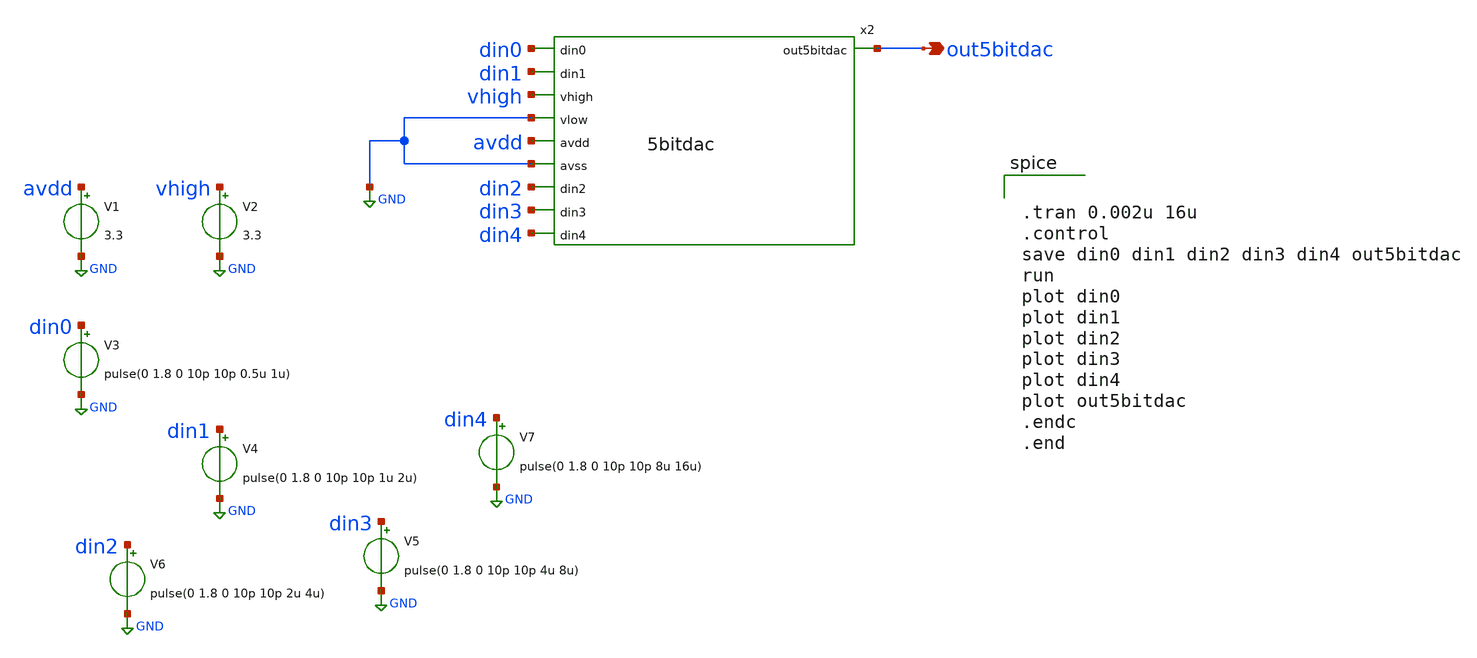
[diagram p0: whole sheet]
** sch_path: xschem/tb_5bitdac_fast.sch
**.subckt tb_5bitdac_fast out5bitdac
*.opin out5bitdac
V1 avdd GND 3.3
V2 vhigh GND 3.3
V3 din0 GND pulse(0 1.8 0 10p 10p 0.5u 1u)
V4 din1 GND pulse(0 1.8 0 10p 10p 1u 2u)
V5 din3 GND pulse(0 1.8 0 10p 10p 4u 8u)
V6 din2 GND pulse(0 1.8 0 10p 10p 2u 4u)
V7 din4 GND pulse(0 1.8 0 10p 10p 8u 16u)
x2 out5bitdac din0 din1 vhigh GND avdd GND din2 din3 din4 5bitdac
**** begin user architecture code

** opencircuitdesign pdks install
.lib $::SKYWATER_MODELS/sky130.lib.spice tt




.tran 0.002u 16u
.control
save din0 din1 din2 din3 din4 out5bitdac
run
plot din0
plot din1
plot din2
plot din3
plot din4
plot out5bitdac
.endc
.end

**** end user architecture code
**.ends

* expanding   symbol:  5bitdac.sym # of pins=10
** sym_path: xschem/5bitdac.sym
** sch_path: xschem/5bitdac.sch
.subckt 5bitdac out5bitdac din0 din1 vhigh vlow avdd avss din2 din3 din4
*.ipin din0
*.ipin din1
*.ipin vhigh
*.ipin vlow
*.ipin avdd
*.ipin avss
*.ipin din2
*.ipin din3
*.opin out5bitdac
*.ipin din4
x1 x1out din0 din1 vhigh net2 avdd avss din2 din3 4bitdac
x2 x2out din0 din1 net1 vlow avdd avss din2 din3 4bitdac
x3 out5bitdac x1out x2out avss avdd din4 switch
XR6 net1 net2 avss sky130_fd_pr__res_high_po_0p35 L=3 mult=1 m=1
.ends


* expanding   symbol:  4bitdac.sym # of pins=9
** sym_path: xschem/4bitdac.sym
** sch_path: xschem/4bitdac.sch
.subckt 4bitdac out4bitdac din0 din1 vhigh vlow avdd avss din2 din3
*.ipin din0
*.ipin din1
*.ipin vhigh
*.ipin vlow
*.ipin avdd
*.ipin avss
*.ipin din2
*.ipin din3
*.opin out4bitdac
x1 x1out din0 din1 vhigh net1 avdd avss din2 3bitdac
x2 x2out din0 din1 net2 vlow avdd avss din2 3bitdac
x3 out4bitdac x1out x2out avss avdd din3 switch
XR6 net2 net1 avss sky130_fd_pr__res_high_po_0p35 L=3 mult=1 m=1
.ends


* expanding   symbol:  switch.sym # of pins=6
** sym_path: xschem/switch.sym
** sch_path: xschem/switch.sch
.subckt switch outsw in1 in2 avss avdd din
*.ipin avss
*.ipin avdd
*.ipin din
*.ipin in1
*.ipin in2
*.opin outsw
XM10 dinbar din avdd avdd sky130_fd_pr__pfet_g5v0d10v5 L=0.5 W=1 nf=1 ad='int((1 + 1)/2) * 1 / 1 * 0.29'
+ as='int((1 + 2)/2) * 1 / 1 * 0.29' pd='2*int((1 + 1)/2) * (1 / 1 + 0.29)' ps='2*int((1 + 2)/2) * (1 / 1 + 0.29)'
+ nrd='0.29 / 1 ' nrs='0.29 / 1 ' sa=0 sb=0 sd=0 mult=1 m=1
XM2 dinbar din avss avss sky130_fd_pr__nfet_g5v0d10v5 L=0.5 W=1 nf=1 ad='int((1 + 1)/2) * 1 / 1 * 0.29'
+ as='int((1 + 2)/2) * 1 / 1 * 0.29' pd='2*int((1 + 1)/2) * (1 / 1 + 0.29)' ps='2*int((1 + 2)/2) * (1 / 1 + 0.29)'
+ nrd='0.29 / 1 ' nrs='0.29 / 1 ' sa=0 sb=0 sd=0 mult=1 m=1
XM1 wc dinbar avdd avdd sky130_fd_pr__pfet_g5v0d10v5 L=0.5 W=1 nf=1 ad='int((1 + 1)/2) * 1 / 1 * 0.29'
+ as='int((1 + 2)/2) * 1 / 1 * 0.29' pd='2*int((1 + 1)/2) * (1 / 1 + 0.29)' ps='2*int((1 + 2)/2) * (1 / 1 + 0.29)'
+ nrd='0.29 / 1 ' nrs='0.29 / 1 ' sa=0 sb=0 sd=0 mult=1 m=1
XM3 wc dinbar avss avss sky130_fd_pr__nfet_g5v0d10v5 L=0.5 W=1 nf=1 ad='int((1 + 1)/2) * 1 / 1 * 0.29'
+ as='int((1 + 2)/2) * 1 / 1 * 0.29' pd='2*int((1 + 1)/2) * (1 / 1 + 0.29)' ps='2*int((1 + 2)/2) * (1 / 1 + 0.29)'
+ nrd='0.29 / 1 ' nrs='0.29 / 1 ' sa=0 sb=0 sd=0 mult=1 m=1
XM5 outsw dinbar in2 avss sky130_fd_pr__nfet_g5v0d10v5 L=0.5 W=1 nf=1 ad='int((1 + 1)/2) * 1 / 1 * 0.29'
+ as='int((1 + 2)/2) * 1 / 1 * 0.29' pd='2*int((1 + 1)/2) * (1 / 1 + 0.29)' ps='2*int((1 + 2)/2) * (1 / 1 + 0.29)'
+ nrd='0.29 / 1 ' nrs='0.29 / 1 ' sa=0 sb=0 sd=0 mult=1 m=1
XM4 outsw dinbar in1 avdd sky130_fd_pr__pfet_g5v0d10v5 L=0.5 W=1 nf=1 ad='int((1 + 1)/2) * 1 / 1 * 0.29'
+ as='int((1 + 2)/2) * 1 / 1 * 0.29' pd='2*int((1 + 1)/2) * (1 / 1 + 0.29)' ps='2*int((1 + 2)/2) * (1 / 1 + 0.29)'
+ nrd='0.29 / 1 ' nrs='0.29 / 1 ' sa=0 sb=0 sd=0 mult=1 m=1
XM11 in2 wc outsw avdd sky130_fd_pr__pfet_g5v0d10v5 L=0.5 W=1 nf=1 ad='int((1 + 1)/2) * 1 / 1 * 0.29'
+ as='int((1 + 2)/2) * 1 / 1 * 0.29' pd='2*int((1 + 1)/2) * (1 / 1 + 0.29)' ps='2*int((1 + 2)/2) * (1 / 1 + 0.29)'
+ nrd='0.29 / 1 ' nrs='0.29 / 1 ' sa=0 sb=0 sd=0 mult=1 m=1
XM12 in1 wc outsw avss sky130_fd_pr__nfet_g5v0d10v5 L=0.5 W=1 nf=1 ad='int((1 + 1)/2) * 1 / 1 * 0.29'
+ as='int((1 + 2)/2) * 1 / 1 * 0.29' pd='2*int((1 + 1)/2) * (1 / 1 + 0.29)' ps='2*int((1 + 2)/2) * (1 / 1 + 0.29)'
+ nrd='0.29 / 1 ' nrs='0.29 / 1 ' sa=0 sb=0 sd=0 mult=1 m=1
.ends


* expanding   symbol:  3bitdac.sym # of pins=8
** sym_path: xschem/3bitdac.sym
** sch_path: xschem/3bitdac.sch
.subckt 3bitdac out3bitdac din0 din1 vrefh vrefl avdd avss din2
*.ipin din0
*.ipin din1
*.ipin vrefh
*.ipin vrefl
*.ipin avdd
*.ipin avss
*.opin out3bitdac
*.ipin din2
x1 x1out din0 vrefh net1 avdd avss din1 2bitdac
x2 x2out din0 net2 vrefl avdd avss din1 2bitdac
x3 out3bitdac x1out x2out avss avdd din2 switch
XR6 net2 net1 avss sky130_fd_pr__res_high_po_0p35 L=3 mult=1 m=1
.ends


* expanding   symbol:  2bitdac.sym # of pins=7
** sym_path: xschem/2bitdac.sym
** sch_path: xschem/2bitdac.sch
.subckt 2bitdac out2bitdac din0 vhigh vlow avdd avss din1
*.ipin din0
*.ipin vhigh
*.ipin vlow
*.ipin avdd
*.ipin avss
*.ipin din1
*.opin out2bitdac
x1 x1_out net1 net2 avss avdd din0 switch
x2 x2_out net3 vlow avss avdd din0 switch
x3 out2bitdac x1_out x2_out avss avdd din1 switch
XR6 net1 vhigh avss sky130_fd_pr__res_high_po_0p35 L=3 mult=1 m=1
XR1 net2 net1 avss sky130_fd_pr__res_high_po_0p35 L=3 mult=1 m=1
XR2 net3 net2 avss sky130_fd_pr__res_high_po_0p35 L=3 mult=1 m=1
XR3 vlow net3 avss sky130_fd_pr__res_high_po_0p35 L=3 mult=1 m=1
.ends

.GLOBAL GND
.end
